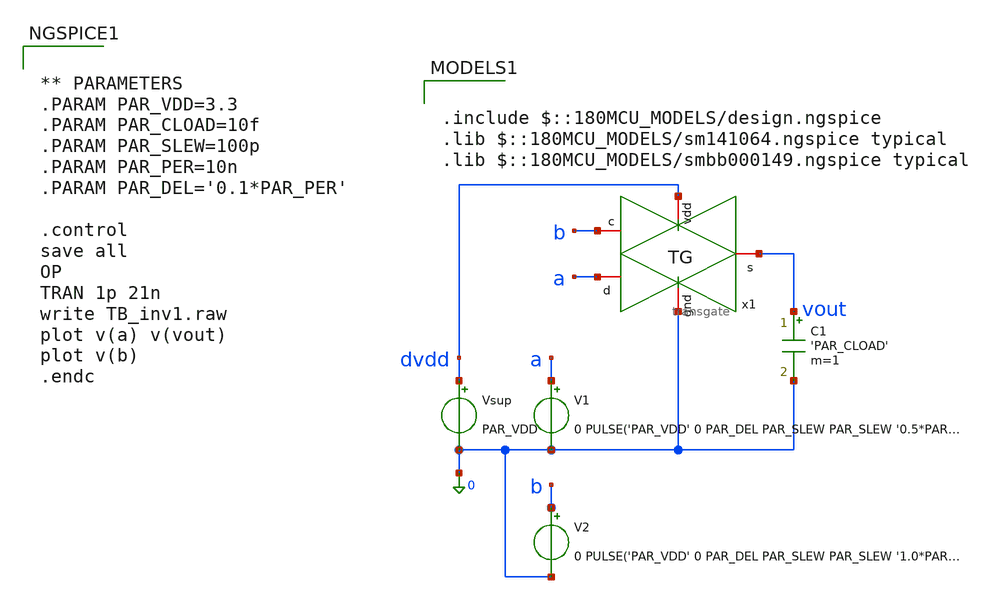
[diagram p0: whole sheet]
** sch_path: src/schematic/TG/TB_transgate.sch
**.subckt TB_transgate
V1 a 0 0 PULSE('PAR_VDD' 0 PAR_DEL PAR_SLEW PAR_SLEW '0.5*PAR_PER' '1.0*PAR_PER')
Vsup dvdd 0 PAR_VDD
C1 vout 0 'PAR_CLOAD' m=1
V2 b 0 0 PULSE('PAR_VDD' 0 PAR_DEL PAR_SLEW PAR_SLEW '1.0*PAR_PER' '2.0*PAR_PER')
x1 dvdd vout a 0 b transgate
**** begin user architecture code

.include $::180MCU_MODELS/design.ngspice
.lib $::180MCU_MODELS/sm141064.ngspice typical
.lib $::180MCU_MODELS/smbb000149.ngspice typical



** PARAMETERS
.PARAM PAR_VDD=3.3
.PARAM PAR_CLOAD=10f
.PARAM PAR_SLEW=100p
.PARAM PAR_PER=10n
.PARAM PAR_DEL='0.1*PAR_PER'

.control
save all
OP
TRAN 1p 21n
write TB_inv1.raw
plot v(a) v(vout)
plot v(b)
.endc


**** end user architecture code
**.ends

* expanding   symbol:  src/schematic/TG/transgate.sym # of pins=5
** sym_path: src/schematic/TG/transgate.sym
** sch_path: src/schematic/TG/transgate.sch
.subckt transgate vdd s d gnd c
*.iopin gnd
*.iopin vdd
*.iopin c
*.ipin d
*.opin s
XM1 d c s gnd nfet_03v3 L=0.28u W=0.22u nf=1 ad='int((nf+1)/2) * W/nf * 0.18u' as='int((nf+2)/2) * W/nf * 0.18u'
+ pd='2*int((nf+1)/2) * (W/nf + 0.18u)' ps='2*int((nf+2)/2) * (W/nf + 0.18u)' nrd='0.18u / W' nrs='0.18u / W'
+ sa=0 sb=0 sd=0 m=1
XM2 d net1 s vdd pfet_03v3 L=0.28u W=0.22u nf=1 ad='int((nf+1)/2) * W/nf * 0.18u' as='int((nf+2)/2) * W/nf * 0.18u'
+ pd='2*int((nf+1)/2) * (W/nf + 0.18u)' ps='2*int((nf+2)/2) * (W/nf + 0.18u)' nrd='0.18u / W' nrs='0.18u / W'
+ sa=0 sb=0 sd=0 m=1
x1 vdd c net1 gnd inverter
.ends


* expanding   symbol:  inverter.sym # of pins=4
** sym_path: src/schematic/TG/inverter.sym
** sch_path: src/schematic/TG/inverter.sch
.subckt inverter vdd vi vo gnd
*.ipin vi
*.opin vo
*.iopin vdd
*.iopin gnd
XM1 vo vi vdd vdd pfet_03v3 L=0.28u W=0.22u nf=1 ad='int((nf+1)/2) * W/nf * 0.18u' as='int((nf+2)/2) * W/nf * 0.18u'
+ pd='2*int((nf+1)/2) * (W/nf + 0.18u)' ps='2*int((nf+2)/2) * (W/nf + 0.18u)' nrd='0.18u / W' nrs='0.18u / W'
+ sa=0 sb=0 sd=0 m=1
XM2 vo vi gnd gnd nfet_03v3 L=0.28u W=0.22u nf=1 ad='int((nf+1)/2) * W/nf * 0.18u' as='int((nf+2)/2) * W/nf * 0.18u'
+ pd='2*int((nf+1)/2) * (W/nf + 0.18u)' ps='2*int((nf+2)/2) * (W/nf + 0.18u)' nrd='0.18u / W' nrs='0.18u / W'
+ sa=0 sb=0 sd=0 m=1
.ends

.end
